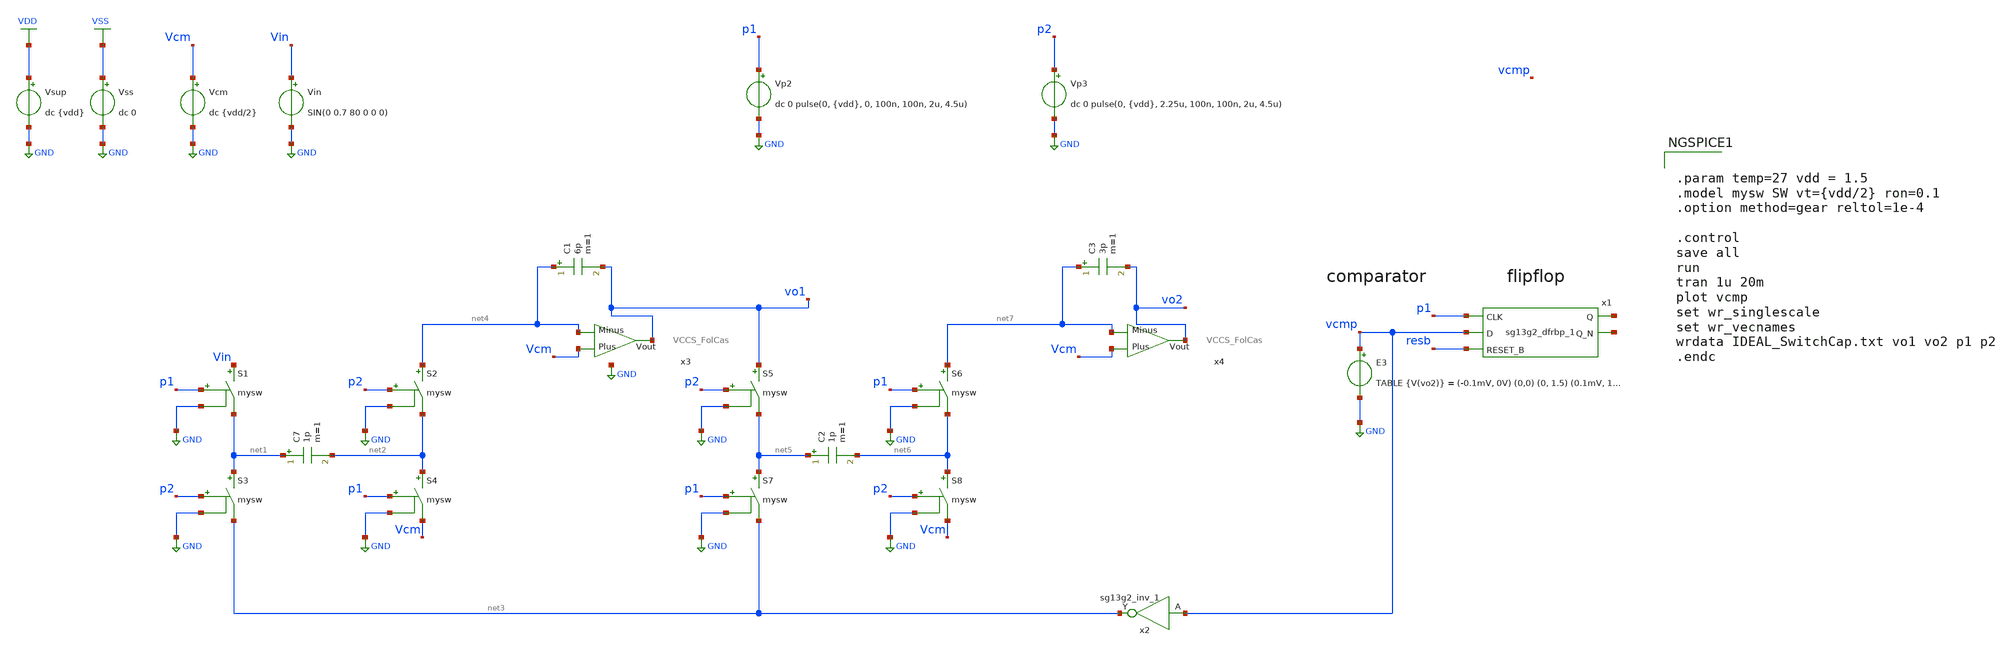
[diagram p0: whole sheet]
** sch_path: DSM/Schematics/Designs_Hrishi/IdealCircuits/IDEAL_DSM_VCCS.sch
* DSM/Schematics/IC_Designs_Hrishi/RealCircuits/Folded Cascode/FoldedCascodeOTA.sch:
* (c) 2024 Hrishikesh, @HSB
**.subckt IDEAL_DSM_VCCS
Vcm Vcm GND dc {vdd/2}
S1 Vin net1 p1 GND mysw
S2 net4 net2 p2 GND mysw
S3 net1 net3 p2 GND mysw
S4 net2 Vcm p1 GND mysw
C7 net1 net2 1p m=1
C1 net4 vo1 6p m=1
S5 vo1 net5 p2 GND mysw
S6 net7 net6 p1 GND mysw
S7 net5 net3 p1 GND mysw
S8 net6 Vcm p2 GND mysw
C2 net5 net6 1p m=1
C3 net7 vo2 3p m=1
x2 net3 vcmp Vdd Vss sg13g2_inv_1
Vsup VDD GND dc {vdd}
Vss VSS GND dc 0
E3 vcmp GND TABLE {V(vo2)} = (-0.1mV, 0V) (0,0) (0, 1.5) (0.1mV, 1.5)
x1 net8 net9 p1 vcmp resb VDD VSS sg13g2_dfrbp_1
Vin Vin GND SIN(0 0.7 80 0 0 0)
x3 Vcm vo1 net4 VCCS_FolCas
x4 Vcm vo2 net7 VCCS_FolCas
Vp2 p1 GND dc 0 pulse(0, {vdd}, 0, 100n, 100n, 2u, 4.5u)
Vp3 p2 GND dc 0 pulse(0, {vdd}, 2.25u, 100n, 100n, 2u, 4.5u)
**** begin user architecture code

.lib $::SG13G2_MODELS/cornerMOSlv.lib mos_tt
.lib $::SG13G2_MODELS/cornerRES.lib res_typ
.inc /foss/pdks/sg13g2/libs.ref/sg13g2_stdcell/spice/sg13g2_stdcell.spice



.param temp=27 vdd = 1.5
.model mysw SW vt={vdd/2} ron=0.1
.option method=gear reltol=1e-4

.control
save all
run
tran 1u 20m
plot vcmp
set wr_singlescale
set wr_vecnames
wrdata IDEAL_SwitchCap.txt vo1 vo2 p1 p2
.endc


**** end user architecture code
**.ends

* expanding   symbol:  sg13g2_stdcells/sg13g2_inv_1.sym # of pins=2
** sym_path: sg13g2_stdcells/sg13g2_inv_1.sym
** sch_path: sg13g2_stdcells/sg13g2_inv_1.sch
.subckt sg13g2_inv_1 Y A VDD VSS
*.opin Y
*.ipin A
*.iopin VDD
*.iopin VSS
XM1 Y A VSS VSS sg13_lv_nmos w=740.00n l=130.00n ng=1 m=1 mm_ok=1
XM2 Y A VDD VDD sg13_lv_pmos w=1.12u l=130.00n ng=1 m=1 mm_ok=1
.ends


* expanding   symbol:  sg13g2_stdcells/sg13g2_dfrbp_1.sym # of pins=5
** sym_path: sg13g2_stdcells/sg13g2_dfrbp_1.sym
** sch_path: sg13g2_stdcells/sg13g2_dfrbp_1.sch
.subckt sg13g2_dfrbp_1 Q Q_N CLK D RESET_B VDD VSS
*.ipin D
*.ipin RESET_B
*.ipin CLK
*.opin Q
*.opin Q_N
*.iopin VDD
*.iopin VSS
XM1 Db D net10 VSS sg13_lv_nmos w=420.00n l=130.00n ng=1 m=1 mm_ok=1
XM2 net10 RESET_B VSS VSS sg13_lv_nmos w=420.00n l=130.00n ng=1 m=1 mm_ok=1
XM3 net1 clkneg net9 VSS sg13_lv_nmos w=420.00n l=130.00n ng=1 m=1 mm_ok=1
XM4 net9 net1 VSS VSS sg13_lv_nmos w=420.00n l=130.00n ng=1 m=1 mm_ok=1
XM5 net1 net1 net5 VSS sg13_lv_nmos w=420.00n l=130.00n ng=1 m=1 mm_ok=1
XM6 net5 RESET_B VSS VSS sg13_lv_nmos w=420.00n l=130.00n ng=1 m=1 mm_ok=1
XM7 Q_N net1 VSS VSS sg13_lv_nmos w=740.00n l=130.00n ng=1 m=1 mm_ok=1
XM8 net2 net1 VSS VSS sg13_lv_nmos w=740.00n l=130.00n ng=1 m=1 mm_ok=1
XM9 Q net2 VSS VSS sg13_lv_nmos w=740.00n l=130.00n ng=1 m=1 mm_ok=1
XM10 clkneg CLK VSS VSS sg13_lv_nmos w=740.00n l=130.00n ng=1 m=1 mm_ok=1
XM11 clkpos clkneg VSS VSS sg13_lv_nmos w=740.00n l=130.00n ng=1 m=1 mm_ok=1
XM12 Db clkneg net3 VSS sg13_lv_nmos w=420.00n l=130.00n ng=1 m=1 mm_ok=1
XM13 net3 clkpos net8 VSS sg13_lv_nmos w=420.00n l=130.00n ng=1 m=1 mm_ok=1
XM14 net8 net3 net4 VSS sg13_lv_nmos w=420.00n l=130.00n ng=1 m=1 mm_ok=1
XM15 net4 RESET_B VSS VSS sg13_lv_nmos w=420.00n l=130.00n ng=1 m=1 mm_ok=1
XM16 net3 net3 VSS VSS sg13_lv_nmos w=740.00n l=130.00n ng=1 m=1 mm_ok=1
XM17 net3 clkpos net1 VSS sg13_lv_nmos w=740.00n l=130.00n ng=1 m=1 mm_ok=1
XM18 Db RESET_B VDD VDD sg13_lv_pmos w=420.00n l=130.00n ng=1 m=1 mm_ok=1
XM19 Db D VDD VDD sg13_lv_pmos w=420.00n l=130.00n ng=1 m=1 mm_ok=1
XM20 net7 net1 VDD VDD sg13_lv_pmos w=420.00n l=130.00n ng=1 m=1 mm_ok=1
XM21 net1 clkpos net7 VDD sg13_lv_pmos w=420.00n l=130.00n ng=1 m=1 mm_ok=1
XM22 net1 net1 VDD VDD sg13_lv_pmos w=420.00n l=130.00n ng=1 m=1 mm_ok=1
XM23 net1 RESET_B VDD VDD sg13_lv_pmos w=420.00n l=130.00n ng=1 m=1 mm_ok=1
XM24 Q_N net1 VDD VDD sg13_lv_pmos w=1.12u l=130.00n ng=1 m=1 mm_ok=1
XM25 net2 net1 VDD VDD sg13_lv_pmos w=1.12u l=130.00n ng=1 m=1 mm_ok=1
XM26 Q net2 VDD VDD sg13_lv_pmos w=1.12u l=130.00n ng=1 m=1 mm_ok=1
XM27 clkneg CLK VDD VDD sg13_lv_pmos w=1.12u l=130.00n ng=1 m=1 mm_ok=1
XM28 clkpos clkneg VDD VDD sg13_lv_pmos w=1.12u l=130.00n ng=1 m=1 mm_ok=1
XM29 Db clkpos net3 VDD sg13_lv_pmos w=420.00n l=130.00n ng=1 m=1 mm_ok=1
XM30 net6 net3 VDD VDD sg13_lv_pmos w=420.00n l=130.00n ng=1 m=1 mm_ok=1
XM31 net3 clkneg net6 VDD sg13_lv_pmos w=420.00n l=130.00n ng=1 m=1 mm_ok=1
XM32 net3 RESET_B VDD VDD sg13_lv_pmos w=420.00n l=130.00n ng=1 m=1 mm_ok=1
XM33 net3 net3 VDD VDD sg13_lv_pmos w=1.000u l=130.00n ng=1 m=1 mm_ok=1
XM34 net3 clkneg net1 VDD sg13_lv_pmos w=1.000u l=130.00n ng=1 m=1 mm_ok=1
.ends


* expanding   symbol:  VCCS_FolCas.sym # of pins=3
** sym_path: DSM/Schematics/Designs_Hrishi/RealCircuits/VCCS_FolCas.sym
** sch_path: DSM/Schematics/Designs_Hrishi/RealCircuits/VCCS_FolCas.sch
.subckt VCCS_FolCas Plus Vout Minus
*.ipin Minus
*.opin Vout
*.ipin Plus
Vdd v_dd GND 1.5
Vss v_ss GND 0
I0 v_dd net1 0.8u
x1 v_dd net1 Plus Minus Vout v_ss FoldedCascodeOTA
.ends


* expanding   symbol:  /foss/designs/CEMS_DSM/DSM/Schematics/IC_Designs_Hrishi/RealCircuits/Folded
*+ Cascode/FoldedCascodeOTA.sym # of pins=6
** sym_path: DSM/Schematics/IC_Designs_Hrishi/RealCircuits/Folded Cascode/FoldedCascodeOTA.sym
** sch_path: DSM/Schematics/IC_Designs_Hrishi/RealCircuits/Folded Cascode/FoldedCascodeOTA.sch
.subckt FoldedCascodeOTA VDD I PLUS MINUS Vout VSS
*.ipin PLUS
*.ipin MINUS
*.opin Vout
*.ipin VDD
*.ipin VSS
*.ipin I
XM1 net2 net4 VDD VDD sg13_lv_pmos w=0.272u l=0.5u ng=1 m=1 mm_ok=1
XM2 net1 PLUS net2 VDD sg13_lv_pmos w=0.136u l=0.5u ng=1 m=1 mm_ok=1
XM3 net6 MINUS net2 VDD sg13_lv_pmos w=0.136u l=0.5u ng=1 m=1 mm_ok=1
XM14 net6 net9 VSS VSS sg13_lv_nmos w=0.30u l=2u ng=1 m=1 mm_ok=1
XM13 Vout I net6 VSS sg13_lv_nmos w=0.15u l=2u ng=1 m=1 mm_ok=1
XM11 net7 I net1 VSS sg13_lv_nmos w=0.15u l=2u ng=1 m=1 mm_ok=1
XM12 net1 net9 VSS VSS sg13_lv_nmos w=0.30u l=2u ng=1 m=1 mm_ok=1
XM5 Vout net3 net5 VDD sg13_lv_pmos w=0.136u l=0.5u ng=1 m=1 mm_ok=1
XM4 net5 net4 VDD VDD sg13_lv_pmos w=0.136u l=0.5u ng=1 m=1 mm_ok=1
XM6 net4 net4 VDD VDD sg13_lv_pmos w=0.136u l=0.5u ng=1 m=1 mm_ok=1
XM8 net3 net3 net4 VDD sg13_lv_pmos w=0.136u l=0.5u ng=1 m=1 mm_ok=1
XM9 net8 net4 VDD VDD sg13_lv_pmos w=0.136u l=0.5u ng=1 m=1 mm_ok=1
XM10 net7 net3 net8 VDD sg13_lv_pmos w=0.136u l=0.5u ng=1 m=1 mm_ok=1
XM16 I I net9 VSS sg13_lv_nmos w=0.15u l=2u ng=1 m=1 mm_ok=1
XM15 net9 net9 VSS VSS sg13_lv_nmos w=0.15u l=2u ng=1 m=1 mm_ok=1
XM7 net3 net9 VSS VSS sg13_lv_nmos w=0.15u l=2u ng=1 m=1 mm_ok=1
XM18 VDD I net10 VSS sg13_lv_nmos w=0.15u l=2u ng=1 m=1 mm_ok=1
XM17 net10 net9 VSS VSS sg13_lv_nmos w=0.15u l=2u ng=1 m=1 mm_ok=1
.ends

.GLOBAL GND
.GLOBAL VDD
.GLOBAL VSS
.end
